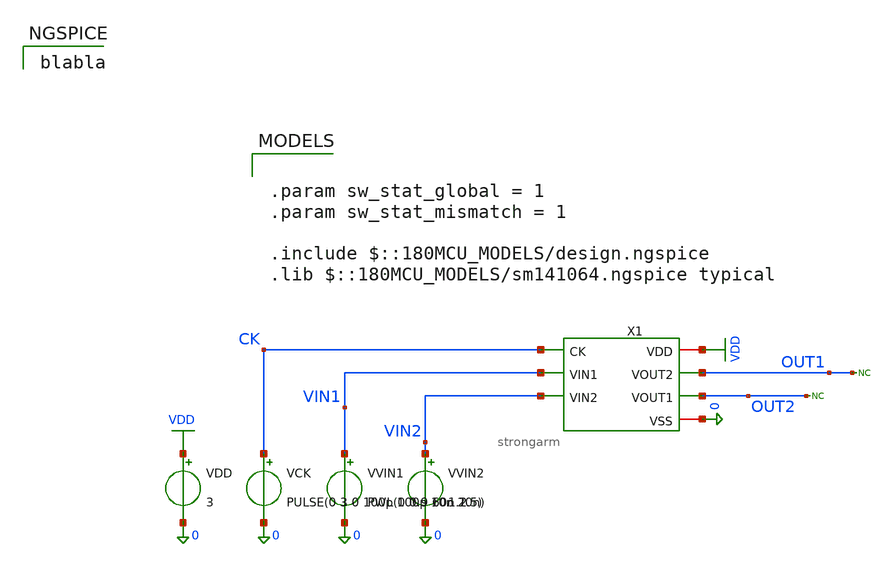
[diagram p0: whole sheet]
** sch_path: comparator/schematic/backup_files/tester_later.sch
**.subckt tester_later
X1 VDD CK OUT1 OUT2 VIN1 VIN2 0 strongarm
VVIN2 VIN2 0 1.2
VVIN1 VIN1 0 PWL(0 0.9 60n 1.5)
VDD VDD 0 3
VCK CK 0 PULSE(0 3 0 100p 100p 10n 20n)
* noconn OUT2
* noconn OUT1
**** begin user architecture code

.param sw_stat_global = 1
.param sw_stat_mismatch = 1

.include $::180MCU_MODELS/design.ngspice
.lib $::180MCU_MODELS/sm141064.ngspice typical


blabla

**** end user architecture code
**.ends

* expanding   symbol:  comparator/schematic/strongarm.sym # of pins=7
** sym_path: comparator/schematic/strongarm.sym
** sch_path: comparator/schematic/strongarm.sch
.subckt strongarm VDD CK VOUT2 VOUT1 VIN1 VIN2 VSS
*.opin VOUT1
*.opin VOUT2
*.ipin VIN1
*.ipin VIN2
*.ipin CK
*.iopin VDD
*.iopin VSS
XM1 VOUT2 VOUT1 net1 net1 nfet_03v3 L=0.28u W=0.22u nf=1 ad='int((nf+1)/2) * W/nf * 0.18u' as='int((nf+2)/2) * W/nf * 0.18u'
+ pd='2*int((nf+1)/2) * (W/nf + 0.18u)' ps='2*int((nf+2)/2) * (W/nf + 0.18u)' nrd='0.18u / W' nrs='0.18u / W'
+ sa=0 sb=0 sd=0 m=1
XM2 VOUT1 VOUT2 VDD VDD pfet_03v3 L=0.28u W=0.22u nf=1 ad='int((nf+1)/2) * W/nf * 0.18u' as='int((nf+2)/2) * W/nf * 0.18u'
+ pd='2*int((nf+1)/2) * (W/nf + 0.18u)' ps='2*int((nf+2)/2) * (W/nf + 0.18u)' nrd='0.18u / W' nrs='0.18u / W'
+ sa=0 sb=0 sd=0 m=1
XM3 VOUT1 CK VDD VDD pfet_03v3 L=0.28u W=0.22u nf=1 ad='int((nf+1)/2) * W/nf * 0.18u' as='int((nf+2)/2) * W/nf * 0.18u'
+ pd='2*int((nf+1)/2) * (W/nf + 0.18u)' ps='2*int((nf+2)/2) * (W/nf + 0.18u)' nrd='0.18u / W' nrs='0.18u / W'
+ sa=0 sb=0 sd=0 m=1
XM4 net3 CK VDD VDD pfet_03v3 L=0.28u W=0.22u nf=1 ad='int((nf+1)/2) * W/nf * 0.18u' as='int((nf+2)/2) * W/nf * 0.18u'
+ pd='2*int((nf+1)/2) * (W/nf + 0.18u)' ps='2*int((nf+2)/2) * (W/nf + 0.18u)' nrd='0.18u / W' nrs='0.18u / W'
+ sa=0 sb=0 sd=0 m=1
XM5 net1 CK VDD VDD pfet_03v3 L=0.28u W=0.22u nf=1 ad='int((nf+1)/2) * W/nf * 0.18u' as='int((nf+2)/2) * W/nf * 0.18u'
+ pd='2*int((nf+1)/2) * (W/nf + 0.18u)' ps='2*int((nf+2)/2) * (W/nf + 0.18u)' nrd='0.18u / W' nrs='0.18u / W'
+ sa=0 sb=0 sd=0 m=1
XM6 VOUT2 CK VDD VDD pfet_03v3 L=0.28u W=0.22u nf=1 ad='int((nf+1)/2) * W/nf * 0.18u' as='int((nf+2)/2) * W/nf * 0.18u'
+ pd='2*int((nf+1)/2) * (W/nf + 0.18u)' ps='2*int((nf+2)/2) * (W/nf + 0.18u)' nrd='0.18u / W' nrs='0.18u / W'
+ sa=0 sb=0 sd=0 m=1
XM7 VOUT2 VOUT1 VDD VDD pfet_03v3 L=0.28u W=0.22u nf=1 ad='int((nf+1)/2) * W/nf * 0.18u' as='int((nf+2)/2) * W/nf * 0.18u'
+ pd='2*int((nf+1)/2) * (W/nf + 0.18u)' ps='2*int((nf+2)/2) * (W/nf + 0.18u)' nrd='0.18u / W' nrs='0.18u / W'
+ sa=0 sb=0 sd=0 m=1
XM8 net1 VIN2 net2 net2 nfet_03v3 L=0.28u W=0.22u nf=1 ad='int((nf+1)/2) * W/nf * 0.18u' as='int((nf+2)/2) * W/nf * 0.18u'
+ pd='2*int((nf+1)/2) * (W/nf + 0.18u)' ps='2*int((nf+2)/2) * (W/nf + 0.18u)' nrd='0.18u / W' nrs='0.18u / W'
+ sa=0 sb=0 sd=0 m=1
XM9 VOUT1 VOUT2 net3 net3 nfet_03v3 L=0.28u W=0.22u nf=1 ad='int((nf+1)/2) * W/nf * 0.18u' as='int((nf+2)/2) * W/nf * 0.18u'
+ pd='2*int((nf+1)/2) * (W/nf + 0.18u)' ps='2*int((nf+2)/2) * (W/nf + 0.18u)' nrd='0.18u / W' nrs='0.18u / W'
+ sa=0 sb=0 sd=0 m=1
XM10 net3 VIN1 net2 net2 nfet_03v3 L=0.28u W=0.22u nf=1 ad='int((nf+1)/2) * W/nf * 0.18u' as='int((nf+2)/2) * W/nf * 0.18u'
+ pd='2*int((nf+1)/2) * (W/nf + 0.18u)' ps='2*int((nf+2)/2) * (W/nf + 0.18u)' nrd='0.18u / W' nrs='0.18u / W'
+ sa=0 sb=0 sd=0 m=1
XM11 net2 CK VSS net2 nfet_03v3 L=0.28u W=0.22u nf=1 ad='int((nf+1)/2) * W/nf * 0.18u' as='int((nf+2)/2) * W/nf * 0.18u'
+ pd='2*int((nf+1)/2) * (W/nf + 0.18u)' ps='2*int((nf+2)/2) * (W/nf + 0.18u)' nrd='0.18u / W' nrs='0.18u / W'
+ sa=0 sb=0 sd=0 m=1
.ends

.GLOBAL VDD
.end
